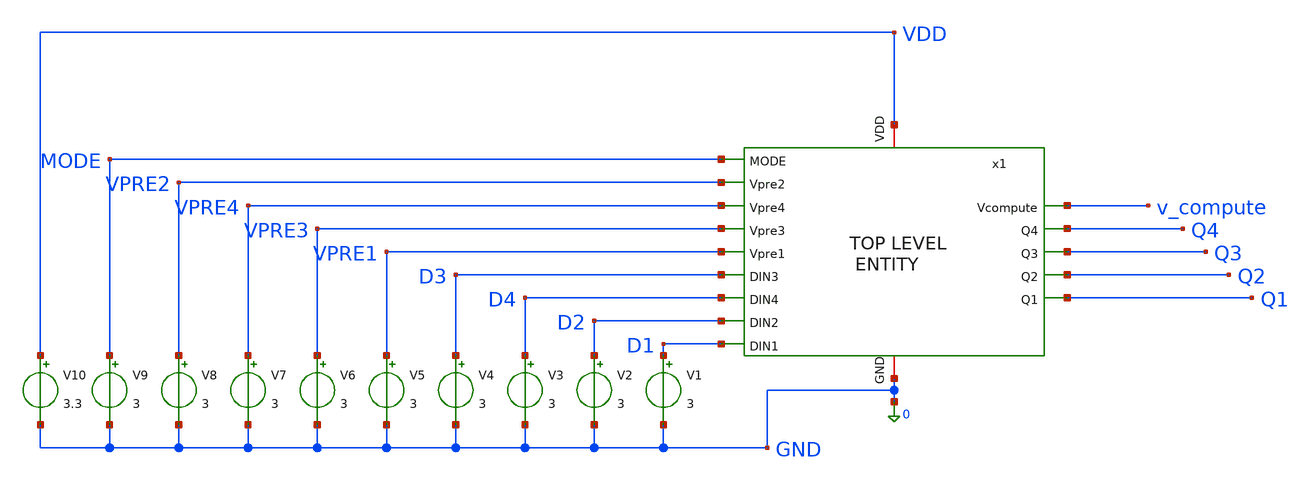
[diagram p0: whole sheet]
** sch_path: src/schematic/INTEGRASI/integrasi_TB.sch
**.subckt integrasi_TB
x1 VDD MODE 0 VPRE2 VPRE4 VPRE3 VPRE1 D3 D4 v_compute Q4 Q3 Q2 Q1 D2 D1 integrasi
V1 D1 0 3
V2 D2 0 3
V3 D4 0 3
V4 D3 0 3
V5 VPRE1 0 3
V6 VPRE3 0 3
V7 VPRE4 0 3
V8 VPRE2 0 3
V9 MODE 0 3
V10 VDD 0 3.3
**.ends
.end
